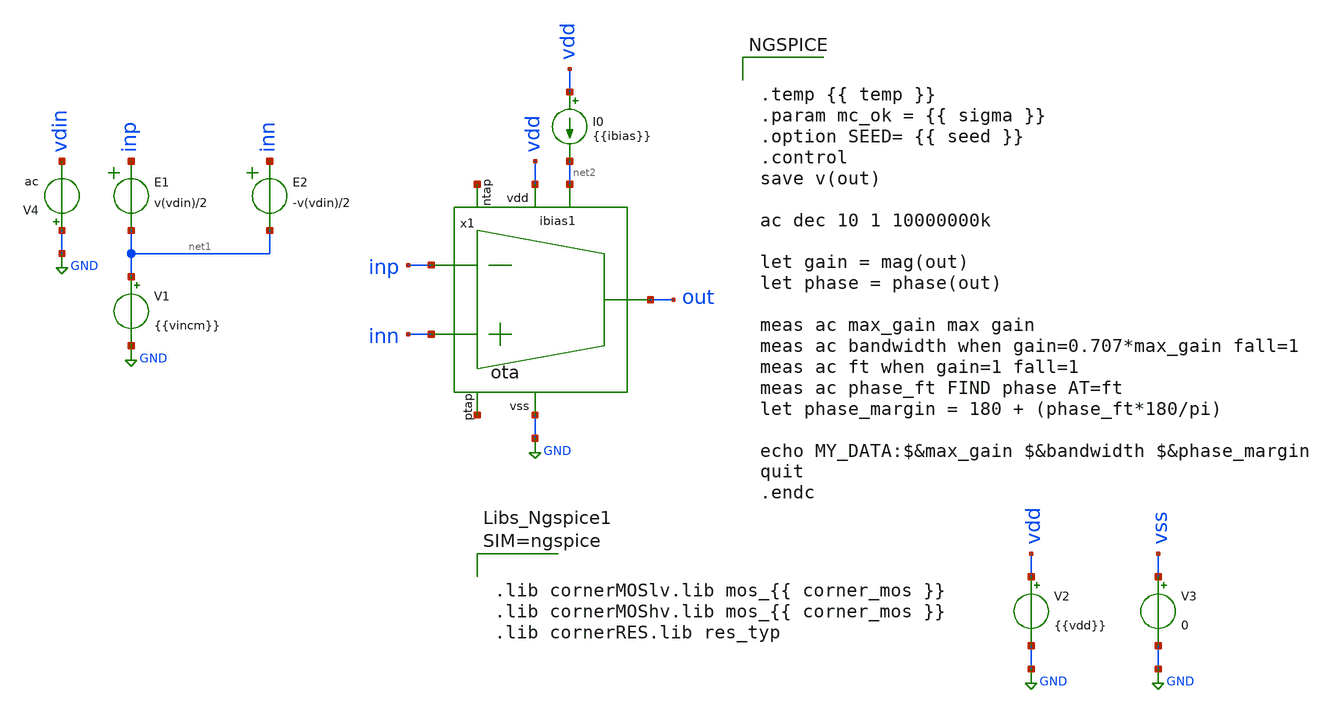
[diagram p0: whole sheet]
** sch_path: examples/ota/tb/tb_ota_gain.sch
**.subckt tb_ota_gain
E1 inp net1 VOL=' v(vdin)/2 '
E2 inn net1 VOL=' -v(vdin)/2 '
V1 net1 GND {{vincm}}
.save i(v1)
V2 vdd GND {{vdd}}
V3 vss GND 0
V4 GND vdin ac
.save i(v4)
I0 vdd net2 {{ibias}}
x1 vdd out inp inn GND net2 net3 net4 ota
**** begin user architecture code


.temp {{ temp }}
.param mc_ok = {{ sigma }}
.option SEED= {{ seed }}
.control
save v(out)

ac dec 10 1 10000000k

let gain = mag(out)
let phase = phase(out)

meas ac max_gain max gain
meas ac bandwidth when gain=0.707*max_gain fall=1
meas ac ft when gain=1 fall=1
meas ac phase_ft FIND phase AT=ft
let phase_margin = 180 + (phase_ft*180/pi)

echo MY_DATA:$&max_gain $&bandwidth $&phase_margin
quit
.endc





.lib cornerMOSlv.lib mos_{{ corner_mos }}
.lib cornerMOShv.lib mos_{{ corner_mos }}
.lib cornerRES.lib res_typ



**** end user architecture code
**.ends

* expanding   symbol:  chipify/examples/ota/sch/ota.sym # of pins=8
** sym_path: examples/ota/sch/ota.sym
** sch_path: examples/ota/sch/ota.sch
.subckt ota vdd out inn inp vss ibias1 ntap ptap
*.ipin inn
*.iopin vdd
*.iopin vss
*.ipin inp
*.ipin ibias1
*.iopin ntap
*.iopin ptap
*.opin out
XM1 net2 inp net1 ptap sg13_lv_nmos w=4u l=1u ng=4 m=1 mm_ok=1
XM2 out inn net1 ptap sg13_lv_nmos w=4u l=1u ng=4 m=1 mm_ok=1
XM3 net1 ibias1 vss ptap sg13_lv_nmos w=8u l=2u ng=4 m=1 mm_ok=1
XM4 ibias1 ibias1 vss ptap sg13_lv_nmos w=8u l=2u ng=4 m=1 mm_ok=1
XM5 net2 net2 vdd ntap sg13_lv_pmos w=2u l=1u ng=1 m=1 mm_ok=1
XM6 out net2 vdd ntap sg13_lv_pmos w=2u l=1u ng=1 m=1 mm_ok=1
XR2 vdd ntap ntap1 R=262.8 w=0.78e-6 l=0.78e-6
XM10 net1 net1 net1 ptap sg13_lv_nmos w=2u l=0.13u ng=2 m=1 mm_ok=1
XR7 vss ptap ptap1 R=262.8 w=0.78e-6 l=0.78e-6
XM51 vss vss vss ptap sg13_lv_nmos w=4u l=0.13u ng=2 m=1 mm_ok=1
XM61 out out out ntap sg13_lv_pmos w=2u l=0.13u ng=2 m=1 mm_ok=1
.ends

.GLOBAL GND
.end
